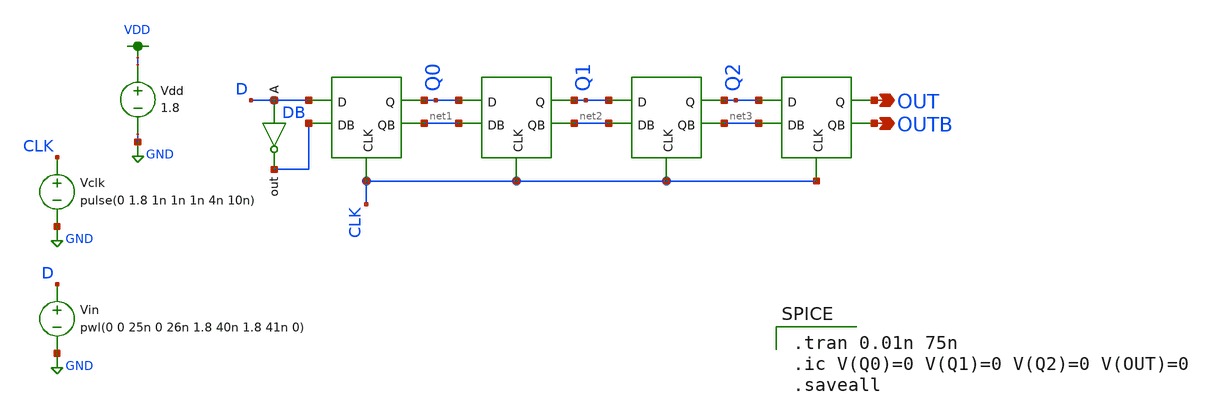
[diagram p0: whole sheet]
** sch_path: MP2/4bitShiftReg.sch
**.subckt 4bitShiftReg OUT OUTB
*.opin OUT
*.opin OUTB
x1 D Q0 DB net1 CLK DFF
x2 Q0 Q1 net1 net2 CLK DFF
x3 Q1 Q2 net2 net3 CLK DFF
x4 Q2 OUT net3 OUTB CLK DFF
x5 DB D INV_mp1
Vdd VDD GND 1.8
Vclk CLK GND pulse(0 1.8 1n 1n 1n 4n 10n)
Vin D GND pwl(0 0 25n 0 26n 1.8 40n 1.8 41n 0)
**** begin user architecture code

.option wnflag=1
.lib ~/skywater/skywater-pdk/libraries/sky130_fd_pr_ngspice/latest/models/sky130.lib.spice tt


.tran 0.01n 75n
.ic V(Q0)=0 V(Q1)=0 V(Q2)=0 V(OUT)=0
.saveall

**** end user architecture code
**.ends

* expanding   symbol:  /home/madvlsi/Documents/MP2/DFF.sym # of pins=5
** sym_path: MP2/DFF.sym
** sch_path: MP2/DFF.sch
.subckt DFF D Q DB QB CLK
*.ipin D
*.ipin DB
*.ipin CLK
*.opin Q
*.opin QB
XM1 net1 CLK D VDD sky130_fd_pr__pfet_01v8 L=0.15 W=1 nf=1 ad='int((nf+1)/2) * W/nf * 0.29' as='int((nf+2)/2) * W/nf * 0.29'
+ pd='2*int((nf+1)/2) * (W/nf + 0.29)' ps='2*int((nf+2)/2) * (W/nf + 0.29)' nrd='0.29 / W' nrs='0.29 / W'
+ sa=0 sb=0 sd=0 mult=1 m=1
XM2 net2 CLK DB VDD sky130_fd_pr__pfet_01v8 L=0.15 W=1 nf=1 ad='int((nf+1)/2) * W/nf * 0.29' as='int((nf+2)/2) * W/nf * 0.29'
+ pd='2*int((nf+1)/2) * (W/nf + 0.29)' ps='2*int((nf+2)/2) * (W/nf + 0.29)' nrd='0.29 / W' nrs='0.29 / W'
+ sa=0 sb=0 sd=0 mult=1 m=1
XM3 Q CLK net1 GND sky130_fd_pr__nfet_01v8 L=0.15 W=1 nf=1 ad='int((nf+1)/2) * W/nf * 0.29' as='int((nf+2)/2) * W/nf * 0.29'
+ pd='2*int((nf+1)/2) * (W/nf + 0.29)' ps='2*int((nf+2)/2) * (W/nf + 0.29)' nrd='0.29 / W' nrs='0.29 / W'
+ sa=0 sb=0 sd=0 mult=1 m=1
XM4 QB CLK net2 GND sky130_fd_pr__nfet_01v8 L=0.15 W=1 nf=1 ad='int((nf+1)/2) * W/nf * 0.29' as='int((nf+2)/2) * W/nf * 0.29'
+ pd='2*int((nf+1)/2) * (W/nf + 0.29)' ps='2*int((nf+2)/2) * (W/nf + 0.29)' nrd='0.29 / W' nrs='0.29 / W'
+ sa=0 sb=0 sd=0 mult=1 m=1
XM5 net3 CLK GND GND sky130_fd_pr__nfet_01v8 L=0.15 W=4 nf=1 ad='int((nf+1)/2) * W/nf * 0.29' as='int((nf+2)/2) * W/nf * 0.29'
+ pd='2*int((nf+1)/2) * (W/nf + 0.29)' ps='2*int((nf+2)/2) * (W/nf + 0.29)' nrd='0.29 / W' nrs='0.29 / W'
+ sa=0 sb=0 sd=0 mult=1 m=1
XM6 net2 net1 net3 GND sky130_fd_pr__nfet_01v8 L=0.15 W=1 nf=1 ad='int((nf+1)/2) * W/nf * 0.29' as='int((nf+2)/2) * W/nf * 0.29'
+ pd='2*int((nf+1)/2) * (W/nf + 0.29)' ps='2*int((nf+2)/2) * (W/nf + 0.29)' nrd='0.29 / W' nrs='0.29 / W'
+ sa=0 sb=0 sd=0 mult=1 m=1
XM7 net1 net2 net3 GND sky130_fd_pr__nfet_01v8 L=0.15 W=1 nf=1 ad='int((nf+1)/2) * W/nf * 0.29' as='int((nf+2)/2) * W/nf * 0.29'
+ pd='2*int((nf+1)/2) * (W/nf + 0.29)' ps='2*int((nf+2)/2) * (W/nf + 0.29)' nrd='0.29 / W' nrs='0.29 / W'
+ sa=0 sb=0 sd=0 mult=1 m=1
XM8 VDD net1 net2 VDD sky130_fd_pr__pfet_01v8 L=0.15 W=1 nf=1 ad='int((nf+1)/2) * W/nf * 0.29' as='int((nf+2)/2) * W/nf * 0.29'
+ pd='2*int((nf+1)/2) * (W/nf + 0.29)' ps='2*int((nf+2)/2) * (W/nf + 0.29)' nrd='0.29 / W' nrs='0.29 / W'
+ sa=0 sb=0 sd=0 mult=1 m=1
XM9 VDD net2 net1 VDD sky130_fd_pr__pfet_01v8 L=0.15 W=1 nf=1 ad='int((nf+1)/2) * W/nf * 0.29' as='int((nf+2)/2) * W/nf * 0.29'
+ pd='2*int((nf+1)/2) * (W/nf + 0.29)' ps='2*int((nf+2)/2) * (W/nf + 0.29)' nrd='0.29 / W' nrs='0.29 / W'
+ sa=0 sb=0 sd=0 mult=1 m=1
XM10 net4 CLK VDD VDD sky130_fd_pr__pfet_01v8 L=0.15 W=4 nf=1 ad='int((nf+1)/2) * W/nf * 0.29' as='int((nf+2)/2) * W/nf * 0.29'
+ pd='2*int((nf+1)/2) * (W/nf + 0.29)' ps='2*int((nf+2)/2) * (W/nf + 0.29)' nrd='0.29 / W' nrs='0.29 / W'
+ sa=0 sb=0 sd=0 mult=1 m=1
XM11 net4 Q QB VDD sky130_fd_pr__pfet_01v8 L=0.15 W=1 nf=1 ad='int((nf+1)/2) * W/nf * 0.29' as='int((nf+2)/2) * W/nf * 0.29'
+ pd='2*int((nf+1)/2) * (W/nf + 0.29)' ps='2*int((nf+2)/2) * (W/nf + 0.29)' nrd='0.29 / W' nrs='0.29 / W'
+ sa=0 sb=0 sd=0 mult=1 m=1
XM12 net4 QB Q VDD sky130_fd_pr__pfet_01v8 L=0.15 W=1 nf=1 ad='int((nf+1)/2) * W/nf * 0.29' as='int((nf+2)/2) * W/nf * 0.29'
+ pd='2*int((nf+1)/2) * (W/nf + 0.29)' ps='2*int((nf+2)/2) * (W/nf + 0.29)' nrd='0.29 / W' nrs='0.29 / W'
+ sa=0 sb=0 sd=0 mult=1 m=1
XM13 QB Q GND GND sky130_fd_pr__nfet_01v8 L=0.15 W=1 nf=1 ad='int((nf+1)/2) * W/nf * 0.29' as='int((nf+2)/2) * W/nf * 0.29'
+ pd='2*int((nf+1)/2) * (W/nf + 0.29)' ps='2*int((nf+2)/2) * (W/nf + 0.29)' nrd='0.29 / W' nrs='0.29 / W'
+ sa=0 sb=0 sd=0 mult=1 m=1
XM14 Q QB GND GND sky130_fd_pr__nfet_01v8 L=0.15 W=1 nf=1 ad='int((nf+1)/2) * W/nf * 0.29' as='int((nf+2)/2) * W/nf * 0.29'
+ pd='2*int((nf+1)/2) * (W/nf + 0.29)' ps='2*int((nf+2)/2) * (W/nf + 0.29)' nrd='0.29 / W' nrs='0.29 / W'
+ sa=0 sb=0 sd=0 mult=1 m=1
.ends


* expanding   symbol:  /home/madvlsi/Documents/MP1/INV_mp1.sym # of pins=2
** sym_path: MP1/INV_mp1.sym
** sch_path: MP1/INV_mp1.sch
.subckt INV_mp1 out A
*.ipin A
*.opin out
XM1 out A VDD VDD sky130_fd_pr__pfet_01v8 L=0.15 W=1 nf=1 ad='int((nf+1)/2) * W/nf * 0.29' as='int((nf+2)/2) * W/nf * 0.29'
+ pd='2*int((nf+1)/2) * (W/nf + 0.29)' ps='2*int((nf+2)/2) * (W/nf + 0.29)' nrd='0.29 / W' nrs='0.29 / W'
+ sa=0 sb=0 sd=0 mult=1 m=1
XM2 out A GND GND sky130_fd_pr__nfet_01v8 L=0.15 W=1 nf=1 ad='int((nf+1)/2) * W/nf * 0.29' as='int((nf+2)/2) * W/nf * 0.29'
+ pd='2*int((nf+1)/2) * (W/nf + 0.29)' ps='2*int((nf+2)/2) * (W/nf + 0.29)' nrd='0.29 / W' nrs='0.29 / W'
+ sa=0 sb=0 sd=0 mult=1 m=1
.ends

.GLOBAL VDD
.GLOBAL GND
.end
